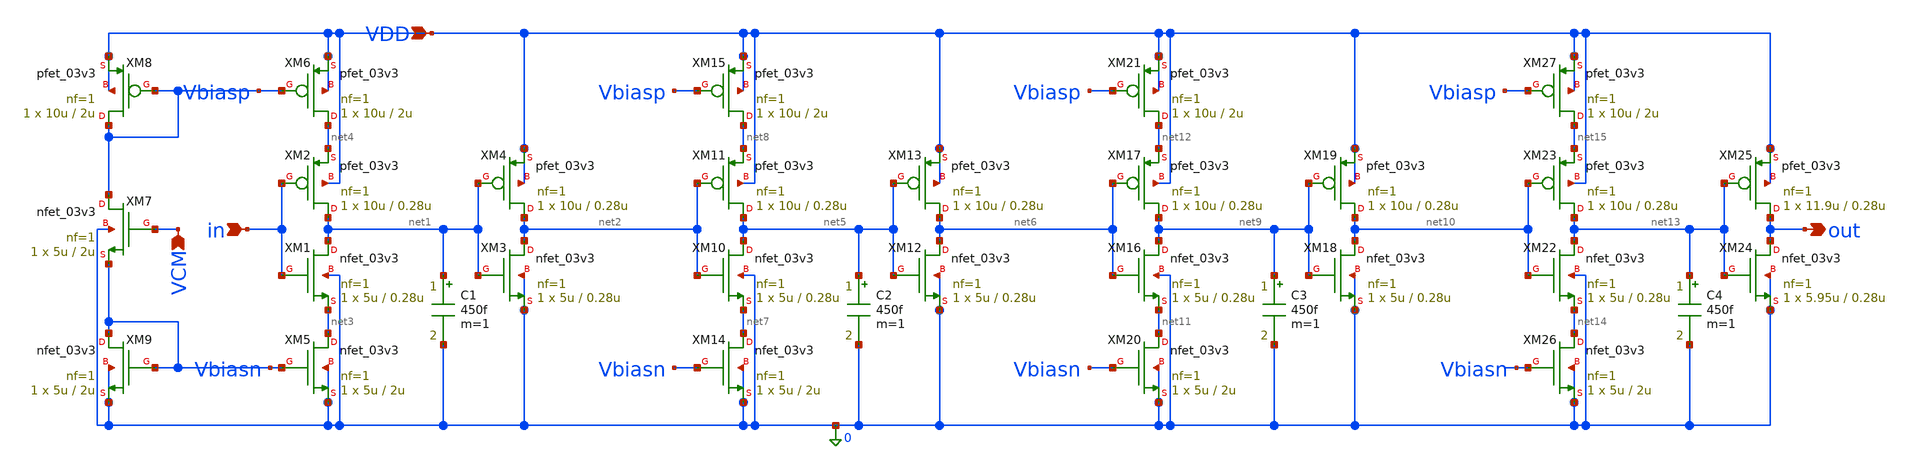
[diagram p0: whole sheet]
** sch_path: Design_Files/IC Design/Schematic/SAR_ADC_BLOCKS/DLY_CELL/DLY_CELL.sch
**.subckt DLY_CELL VDD in VCM out
*.ipin VDD
*.ipin in
*.ipin VCM
*.opin out
XM1 net1 in net3 0 nfet_03v3 L=0.28u W=5u nf=1 ad='int((nf+1)/2) * W/nf * 0.18u' as='int((nf+2)/2) * W/nf * 0.18u'
+ pd='2*int((nf+1)/2) * (W/nf + 0.18u)' ps='2*int((nf+2)/2) * (W/nf + 0.18u)' nrd='0.18u / W' nrs='0.18u / W'
+ sa=0 sb=0 sd=0 m=1
XM2 net1 in net4 VDD pfet_03v3 L=0.28u W=10u nf=1 ad='int((nf+1)/2) * W/nf * 0.18u' as='int((nf+2)/2) * W/nf * 0.18u'
+ pd='2*int((nf+1)/2) * (W/nf + 0.18u)' ps='2*int((nf+2)/2) * (W/nf + 0.18u)' nrd='0.18u / W' nrs='0.18u / W'
+ sa=0 sb=0 sd=0 m=1
XM3 net2 net1 0 0 nfet_03v3 L=0.28u W=5u nf=1 ad='int((nf+1)/2) * W/nf * 0.18u' as='int((nf+2)/2) * W/nf * 0.18u'
+ pd='2*int((nf+1)/2) * (W/nf + 0.18u)' ps='2*int((nf+2)/2) * (W/nf + 0.18u)' nrd='0.18u / W' nrs='0.18u / W'
+ sa=0 sb=0 sd=0 m=1
XM4 net2 net1 VDD VDD pfet_03v3 L=0.28u W=10u nf=1 ad='int((nf+1)/2) * W/nf * 0.18u' as='int((nf+2)/2) * W/nf * 0.18u'
+ pd='2*int((nf+1)/2) * (W/nf + 0.18u)' ps='2*int((nf+2)/2) * (W/nf + 0.18u)' nrd='0.18u / W' nrs='0.18u / W'
+ sa=0 sb=0 sd=0 m=1
XM5 net3 Vbiasn 0 0 nfet_03v3 L=2u W=5u nf=1 ad='int((nf+1)/2) * W/nf * 0.18u' as='int((nf+2)/2) * W/nf * 0.18u'
+ pd='2*int((nf+1)/2) * (W/nf + 0.18u)' ps='2*int((nf+2)/2) * (W/nf + 0.18u)' nrd='0.18u / W' nrs='0.18u / W'
+ sa=0 sb=0 sd=0 m=1
XM6 net4 Vbiasp VDD VDD pfet_03v3 L=2u W=10u nf=1 ad='int((nf+1)/2) * W/nf * 0.18u' as='int((nf+2)/2) * W/nf * 0.18u'
+ pd='2*int((nf+1)/2) * (W/nf + 0.18u)' ps='2*int((nf+2)/2) * (W/nf + 0.18u)' nrd='0.18u / W' nrs='0.18u / W'
+ sa=0 sb=0 sd=0 m=1
XM7 Vbiasp VCM Vbiasn 0 nfet_03v3 L=2u W=5u nf=1 ad='int((nf+1)/2) * W/nf * 0.18u' as='int((nf+2)/2) * W/nf * 0.18u'
+ pd='2*int((nf+1)/2) * (W/nf + 0.18u)' ps='2*int((nf+2)/2) * (W/nf + 0.18u)' nrd='0.18u / W' nrs='0.18u / W'
+ sa=0 sb=0 sd=0 m=1
XM8 Vbiasp Vbiasp VDD VDD pfet_03v3 L=2u W=10u nf=1 ad='int((nf+1)/2) * W/nf * 0.18u' as='int((nf+2)/2) * W/nf * 0.18u'
+ pd='2*int((nf+1)/2) * (W/nf + 0.18u)' ps='2*int((nf+2)/2) * (W/nf + 0.18u)' nrd='0.18u / W' nrs='0.18u / W'
+ sa=0 sb=0 sd=0 m=1
XM9 Vbiasn Vbiasn 0 0 nfet_03v3 L=2u W=5u nf=1 ad='int((nf+1)/2) * W/nf * 0.18u' as='int((nf+2)/2) * W/nf * 0.18u'
+ pd='2*int((nf+1)/2) * (W/nf + 0.18u)' ps='2*int((nf+2)/2) * (W/nf + 0.18u)' nrd='0.18u / W' nrs='0.18u / W'
+ sa=0 sb=0 sd=0 m=1
C1 net1 0 450f m=1
C2 net5 0 450f m=1
C3 net9 0 450f m=1
C4 net13 0 450f m=1
XM14 net7 Vbiasn 0 0 nfet_03v3 L=2u W=5u nf=1 ad='int((nf+1)/2) * W/nf * 0.18u' as='int((nf+2)/2) * W/nf * 0.18u'
+ pd='2*int((nf+1)/2) * (W/nf + 0.18u)' ps='2*int((nf+2)/2) * (W/nf + 0.18u)' nrd='0.18u / W' nrs='0.18u / W'
+ sa=0 sb=0 sd=0 m=1
XM15 net8 Vbiasp VDD VDD pfet_03v3 L=2u W=10u nf=1 ad='int((nf+1)/2) * W/nf * 0.18u' as='int((nf+2)/2) * W/nf * 0.18u'
+ pd='2*int((nf+1)/2) * (W/nf + 0.18u)' ps='2*int((nf+2)/2) * (W/nf + 0.18u)' nrd='0.18u / W' nrs='0.18u / W'
+ sa=0 sb=0 sd=0 m=1
XM20 net11 Vbiasn 0 0 nfet_03v3 L=2u W=5u nf=1 ad='int((nf+1)/2) * W/nf * 0.18u' as='int((nf+2)/2) * W/nf * 0.18u'
+ pd='2*int((nf+1)/2) * (W/nf + 0.18u)' ps='2*int((nf+2)/2) * (W/nf + 0.18u)' nrd='0.18u / W' nrs='0.18u / W'
+ sa=0 sb=0 sd=0 m=1
XM21 net12 Vbiasp VDD VDD pfet_03v3 L=2u W=10u nf=1 ad='int((nf+1)/2) * W/nf * 0.18u' as='int((nf+2)/2) * W/nf * 0.18u'
+ pd='2*int((nf+1)/2) * (W/nf + 0.18u)' ps='2*int((nf+2)/2) * (W/nf + 0.18u)' nrd='0.18u / W' nrs='0.18u / W'
+ sa=0 sb=0 sd=0 m=1
XM26 net14 Vbiasn 0 0 nfet_03v3 L=2u W=5u nf=1 ad='int((nf+1)/2) * W/nf * 0.18u' as='int((nf+2)/2) * W/nf * 0.18u'
+ pd='2*int((nf+1)/2) * (W/nf + 0.18u)' ps='2*int((nf+2)/2) * (W/nf + 0.18u)' nrd='0.18u / W' nrs='0.18u / W'
+ sa=0 sb=0 sd=0 m=1
XM27 net15 Vbiasp VDD VDD pfet_03v3 L=2u W=10u nf=1 ad='int((nf+1)/2) * W/nf * 0.18u' as='int((nf+2)/2) * W/nf * 0.18u'
+ pd='2*int((nf+1)/2) * (W/nf + 0.18u)' ps='2*int((nf+2)/2) * (W/nf + 0.18u)' nrd='0.18u / W' nrs='0.18u / W'
+ sa=0 sb=0 sd=0 m=1
XM10 net5 net2 net7 0 nfet_03v3 L=0.28u W=5u nf=1 ad='int((nf+1)/2) * W/nf * 0.18u' as='int((nf+2)/2) * W/nf * 0.18u'
+ pd='2*int((nf+1)/2) * (W/nf + 0.18u)' ps='2*int((nf+2)/2) * (W/nf + 0.18u)' nrd='0.18u / W' nrs='0.18u / W'
+ sa=0 sb=0 sd=0 m=1
XM11 net5 net2 net8 VDD pfet_03v3 L=0.28u W=10u nf=1 ad='int((nf+1)/2) * W/nf * 0.18u' as='int((nf+2)/2) * W/nf * 0.18u'
+ pd='2*int((nf+1)/2) * (W/nf + 0.18u)' ps='2*int((nf+2)/2) * (W/nf + 0.18u)' nrd='0.18u / W' nrs='0.18u / W'
+ sa=0 sb=0 sd=0 m=1
XM12 net6 net5 0 0 nfet_03v3 L=0.28u W=5u nf=1 ad='int((nf+1)/2) * W/nf * 0.18u' as='int((nf+2)/2) * W/nf * 0.18u'
+ pd='2*int((nf+1)/2) * (W/nf + 0.18u)' ps='2*int((nf+2)/2) * (W/nf + 0.18u)' nrd='0.18u / W' nrs='0.18u / W'
+ sa=0 sb=0 sd=0 m=1
XM13 net6 net5 VDD VDD pfet_03v3 L=0.28u W=10u nf=1 ad='int((nf+1)/2) * W/nf * 0.18u' as='int((nf+2)/2) * W/nf * 0.18u'
+ pd='2*int((nf+1)/2) * (W/nf + 0.18u)' ps='2*int((nf+2)/2) * (W/nf + 0.18u)' nrd='0.18u / W' nrs='0.18u / W'
+ sa=0 sb=0 sd=0 m=1
XM16 net9 net6 net11 0 nfet_03v3 L=0.28u W=5u nf=1 ad='int((nf+1)/2) * W/nf * 0.18u' as='int((nf+2)/2) * W/nf * 0.18u'
+ pd='2*int((nf+1)/2) * (W/nf + 0.18u)' ps='2*int((nf+2)/2) * (W/nf + 0.18u)' nrd='0.18u / W' nrs='0.18u / W'
+ sa=0 sb=0 sd=0 m=1
XM17 net9 net6 net12 VDD pfet_03v3 L=0.28u W=10u nf=1 ad='int((nf+1)/2) * W/nf * 0.18u' as='int((nf+2)/2) * W/nf * 0.18u'
+ pd='2*int((nf+1)/2) * (W/nf + 0.18u)' ps='2*int((nf+2)/2) * (W/nf + 0.18u)' nrd='0.18u / W' nrs='0.18u / W'
+ sa=0 sb=0 sd=0 m=1
XM18 net10 net9 0 0 nfet_03v3 L=0.28u W=5u nf=1 ad='int((nf+1)/2) * W/nf * 0.18u' as='int((nf+2)/2) * W/nf * 0.18u'
+ pd='2*int((nf+1)/2) * (W/nf + 0.18u)' ps='2*int((nf+2)/2) * (W/nf + 0.18u)' nrd='0.18u / W' nrs='0.18u / W'
+ sa=0 sb=0 sd=0 m=1
XM19 net10 net9 VDD VDD pfet_03v3 L=0.28u W=10u nf=1 ad='int((nf+1)/2) * W/nf * 0.18u' as='int((nf+2)/2) * W/nf * 0.18u'
+ pd='2*int((nf+1)/2) * (W/nf + 0.18u)' ps='2*int((nf+2)/2) * (W/nf + 0.18u)' nrd='0.18u / W' nrs='0.18u / W'
+ sa=0 sb=0 sd=0 m=1
XM22 net13 net10 net14 0 nfet_03v3 L=0.28u W=5u nf=1 ad='int((nf+1)/2) * W/nf * 0.18u' as='int((nf+2)/2) * W/nf * 0.18u'
+ pd='2*int((nf+1)/2) * (W/nf + 0.18u)' ps='2*int((nf+2)/2) * (W/nf + 0.18u)' nrd='0.18u / W' nrs='0.18u / W'
+ sa=0 sb=0 sd=0 m=1
XM23 net13 net10 net15 VDD pfet_03v3 L=0.28u W=10u nf=1 ad='int((nf+1)/2) * W/nf * 0.18u' as='int((nf+2)/2) * W/nf * 0.18u'
+ pd='2*int((nf+1)/2) * (W/nf + 0.18u)' ps='2*int((nf+2)/2) * (W/nf + 0.18u)' nrd='0.18u / W' nrs='0.18u / W'
+ sa=0 sb=0 sd=0 m=1
XM24 out net13 0 0 nfet_03v3 L=0.28u W=5.95u nf=1 ad='int((nf+1)/2) * W/nf * 0.18u' as='int((nf+2)/2) * W/nf * 0.18u'
+ pd='2*int((nf+1)/2) * (W/nf + 0.18u)' ps='2*int((nf+2)/2) * (W/nf + 0.18u)' nrd='0.18u / W' nrs='0.18u / W'
+ sa=0 sb=0 sd=0 m=1
XM25 out net13 VDD VDD pfet_03v3 L=0.28u W=11.9u nf=1 ad='int((nf+1)/2) * W/nf * 0.18u' as='int((nf+2)/2) * W/nf * 0.18u'
+ pd='2*int((nf+1)/2) * (W/nf + 0.18u)' ps='2*int((nf+2)/2) * (W/nf + 0.18u)' nrd='0.18u / W' nrs='0.18u / W'
+ sa=0 sb=0 sd=0 m=1
**.ends
.end
